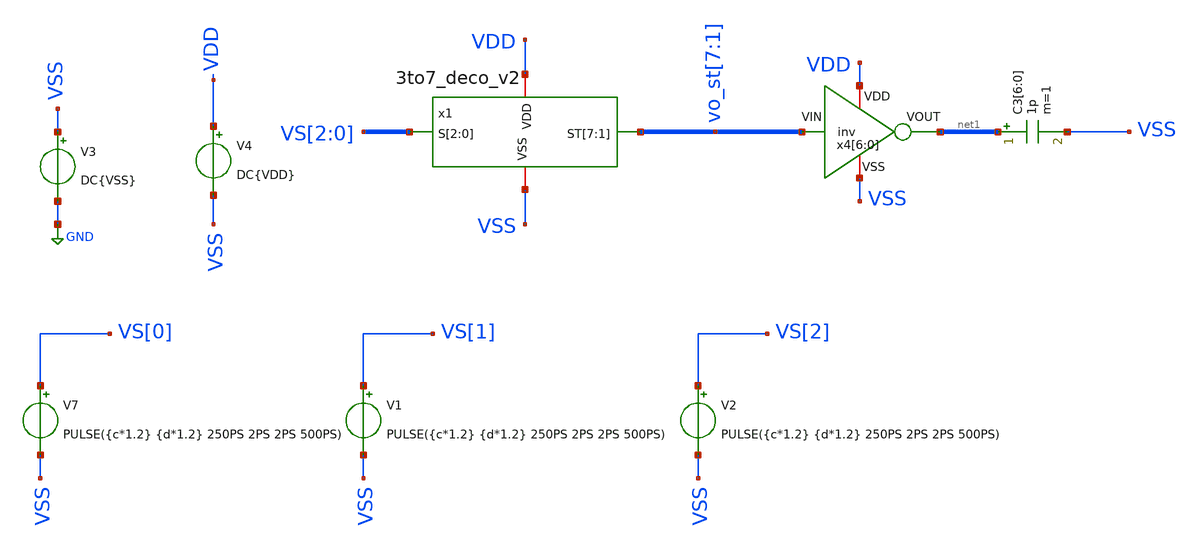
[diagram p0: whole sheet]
** sch_path: BinarytoThermo/tb_3to7_deco_v2_tran.sch
**.subckt tb_3to7_deco_v2_tran
V7 VS[0] VSS PULSE({c*1.2} {d*1.2} 250PS 2PS 2PS 500PS)
V1 VS[1] VSS PULSE({c*1.2} {d*1.2} 250PS 2PS 2PS 500PS)
V2 VS[2] VSS PULSE({c*1.2} {d*1.2} 250PS 2PS 2PS 500PS)
V3 VSS GND DC{VSS}
V4 VDD VSS DC{VDD}
x4[6] VDD net1[6] vo_st[7] VSS inv
x4[5] VDD net1[5] vo_st[6] VSS inv
x4[4] VDD net1[4] vo_st[5] VSS inv
x4[3] VDD net1[3] vo_st[4] VSS inv
x4[2] VDD net1[2] vo_st[3] VSS inv
x4[1] VDD net1[1] vo_st[2] VSS inv
x4[0] VDD net1[0] vo_st[1] VSS inv
C3[6] net1[6] VSS 1p m=1
C3[5] net1[5] VSS 1p m=1
C3[4] net1[4] VSS 1p m=1
C3[3] net1[3] VSS 1p m=1
C3[2] net1[2] VSS 1p m=1
C3[1] net1[1] VSS 1p m=1
C3[0] net1[0] VSS 1p m=1
x1 vo_st[7] vo_st[6] vo_st[5] vo_st[4] vo_st[3] vo_st[2] vo_st[1] VS[2] VS[1] VS[0] VDD VSS
+ 3to7_deco_v2
**** begin user architecture code



* Circuit Parameters
.param vdd = 1.2
.param vss = 0.0
.param a=0
.param b=0
.param c=0
.param d=1
.param Tclk = 500P
.options TEMP = 65.0

* Include Models
.lib /opt/pdks/ihp-sg13g2/libs.tech/ngspice/models/cornerMOSlv.lib mos_tt
.lib /opt/pdks/ihp-sg13g2/libs.tech/ngspice/models/cornerMOShv.lib mos_tt
.lib /opt/pdks/ihp-sg13g2/libs.tech/ngspice/models/cornerHBT.lib hbt_typ
.lib /opt/pdks/ihp-sg13g2/libs.tech/ngspice/models/cornerRES.lib res_typ


* OP Parameters & Singals to save
.save all

*Simulations
.control
set output_path = tb_bin2thermo_tran/
	* Desde (s3,s4)=00 a 01
	tran 0.2PS 750PS
	setplot tran1
	plot vs3 vs4 vo_s3t ylabel vout xlabel vin
	set filetype = ascii
	write {$output_path}tran00to01.raw V(vo_s3t) V(vs3) V(vs4)
	* Desde (s3,s4)=00 a 10
	alterparam d=0
	alterparam b=1
	reset
	tran 0.2PS 750PS
	setplot tran2
	plot vs3 vs4 vo_s2t vo_s3t ylabel vout xlabel vin
	set filetype = ascii
	write {$output_path}tran00to10.raw V(vo_s2t) V(vo_s3t) V(vs3) V(vs4)
	* Desde (s3,s4)=00 a 11
	alterparam d = 1
	reset
	tran 0.2PS 750PS
	setplot tran3
	plot vs3 vs4 vo_s1t vo_s2t vo_s3t ylabel vout xlabel vin
	set filetype = ascii
	write {$output_path}tran00to11.raw V(vo_s1t) V(vo_s2t) V(vo_s3t) V(vs3) V(vs4)
	* Desde (s3,s4)=01 a 10
	alterparam c=1
	alterparam d=0
	reset
	tran 0.2PS 750PS
	setplot tran4
	plot vs3 vs4 vo_s2t ylabel vout xlabel vin
	set filetype = ascii
	write {$output_path}tran01to10.raw V(vo_s2t) V(vs3) V(vs4)
	* Desde (s3,s4)=01 a 11
	alterparam a=0
	alterparam b=1
	alterparam d=1
	reset
	tran 0.2PS 750PS
	setplot tran5
	plot vs3 vs4 vo_s1t vo_s2t ylabel vout xlabel vin
	set filetype = ascii
	write {$output_path}tran01to11.raw V(vo_s1t) V(vo_s2t) V(vs3) V(vs4)
	* Desde (s3,s4)=10 a 11
	alterparam a=1
	alterparam c=0
	alterparam d=1
	reset
	tran 0.2PS 750PS
	setplot tran6
	plot vs3 vs4 vo_s1t ylabel vout xlabel vin ylimit 0 1.2
	set filetype = ascii
	write {$output_path}tran10to11.raw V(vo_s1t) V(vs3) V(vs4)
.endc
.end

**** end user architecture code
**.ends
.GLOBAL GND
.end
